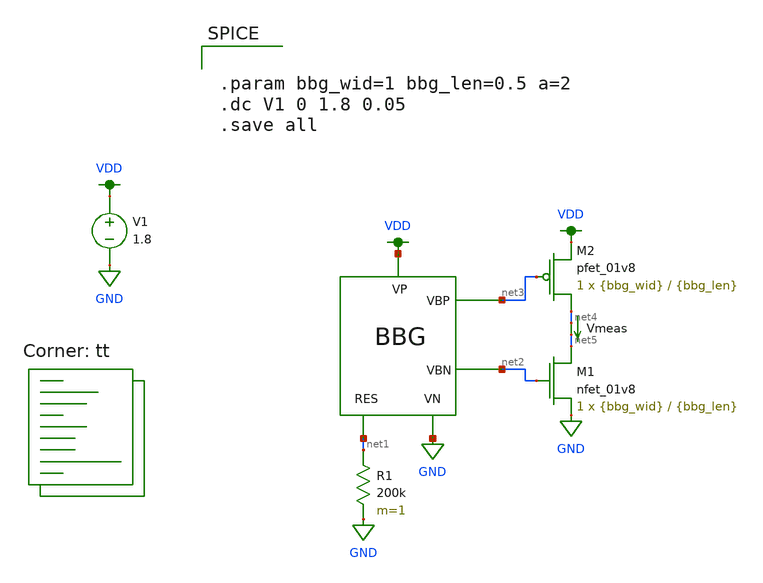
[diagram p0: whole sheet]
** sch_path: test_bbg.sch
**.subckt test_bbg
R1 net1 GND 200k m=1
V1 VDD GND 1.8
XM1 net5 net2 GND GND sky130_fd_pr__nfet_01v8 L={bbg_len} W={bbg_wid} nf=1 ad='int((nf+1)/2) * W/nf * 0.29'
+ as='int((nf+2)/2) * W/nf * 0.29' pd='2*int((nf+1)/2) * (W/nf + 0.29)' ps='2*int((nf+2)/2) * (W/nf + 0.29)'
+ nrd='0.29 / W' nrs='0.29 / W' sa=0 sb=0 sd=0 mult=1 m=1
XM2 net4 net3 VDD VDD sky130_fd_pr__pfet_01v8 L={bbg_len} W={bbg_wid} nf=1 ad='int((nf+1)/2) * W/nf * 0.29'
+ as='int((nf+2)/2) * W/nf * 0.29' pd='2*int((nf+1)/2) * (W/nf + 0.29)' ps='2*int((nf+2)/2) * (W/nf + 0.29)'
+ nrd='0.29 / W' nrs='0.29 / W' sa=0 sb=0 sd=0 mult=1 m=1
Vmeas net4 net5 0
.save i(vmeas)
X1 VDD net1 GND net3 net2 bbg
**** begin user architecture code


.param bbg_wid=1 bbg_len=0.5 a=2
.dc V1 0 1.8 0.05
.save all

.lib $::SKYWATER_MODELS/sky130.lib.spice tt
**** end user architecture code
**.ends

* expanding   symbol:  bbg.sym # of pins=5
** sym_path: bbg.sym
** sch_path: bbg.sch
.subckt bbg VP RES VN VBP VBN
*.iopin VP
*.iopin VN
*.iopin RES
*.opin VBP
*.opin VBN
XM1 net1 net1 RES VN sky130_fd_pr__nfet_01v8 L={bbg_len} W={a}*{bbg_wid} nf=1 ad='int((nf+1)/2) * W/nf * 0.29'
+ as='int((nf+2)/2) * W/nf * 0.29' pd='2*int((nf+1)/2) * (W/nf + 0.29)' ps='2*int((nf+2)/2) * (W/nf + 0.29)'
+ nrd='0.29 / W' nrs='0.29 / W' sa=0 sb=0 sd=0 mult=1 m=1
XM2 net2 net1 VN VN sky130_fd_pr__nfet_01v8 L={bbg_len} W={bbg_wid} nf=1 ad='int((nf+1)/2) * W/nf * 0.29'
+ as='int((nf+2)/2) * W/nf * 0.29' pd='2*int((nf+1)/2) * (W/nf + 0.29)' ps='2*int((nf+2)/2) * (W/nf + 0.29)'
+ nrd='0.29 / W' nrs='0.29 / W' sa=0 sb=0 sd=0 mult=1 m=1
XM3 net1 VBP VP VP sky130_fd_pr__pfet_01v8 L={bbg_len} W={bbg_wid} nf=1 ad='int((nf+1)/2) * W/nf * 0.29'
+ as='int((nf+2)/2) * W/nf * 0.29' pd='2*int((nf+1)/2) * (W/nf + 0.29)' ps='2*int((nf+2)/2) * (W/nf + 0.29)'
+ nrd='0.29 / W' nrs='0.29 / W' sa=0 sb=0 sd=0 mult=1 m=1
Vmeas net3 VBN 0
.save i(vmeas)
XM6 VN VBN VBP VN sky130_fd_pr__nfet_01v8 L={bbg_len} W={bbg_wid} nf=1 ad='int((nf+1)/2) * W/nf * 0.29'
+ as='int((nf+2)/2) * W/nf * 0.29' pd='2*int((nf+1)/2) * (W/nf + 0.29)' ps='2*int((nf+2)/2) * (W/nf + 0.29)'
+ nrd='0.29 / W' nrs='0.29 / W' sa=0 sb=0 sd=0 mult=1 m=1
XM7 VBN VBN VN VN sky130_fd_pr__nfet_01v8 L={bbg_len} W={bbg_wid} nf=1 ad='int((nf+1)/2) * W/nf * 0.29'
+ as='int((nf+2)/2) * W/nf * 0.29' pd='2*int((nf+1)/2) * (W/nf + 0.29)' ps='2*int((nf+2)/2) * (W/nf + 0.29)'
+ nrd='0.29 / W' nrs='0.29 / W' sa=0 sb=0 sd=0 mult=1 m=1
XM4 net2 net2 VP VP sky130_fd_pr__pfet_01v8 L={bbg_len} W={bbg_wid} nf=1 ad='int((nf+1)/2) * W/nf * 0.29'
+ as='int((nf+2)/2) * W/nf * 0.29' pd='2*int((nf+1)/2) * (W/nf + 0.29)' ps='2*int((nf+2)/2) * (W/nf + 0.29)'
+ nrd='0.29 / W' nrs='0.29 / W' sa=0 sb=0 sd=0 mult=1 m=1
XM5 VP net2 VBP VP sky130_fd_pr__pfet_01v8 L={bbg_len} W={bbg_wid} nf=1 ad='int((nf+1)/2) * W/nf * 0.29'
+ as='int((nf+2)/2) * W/nf * 0.29' pd='2*int((nf+1)/2) * (W/nf + 0.29)' ps='2*int((nf+2)/2) * (W/nf + 0.29)'
+ nrd='0.29 / W' nrs='0.29 / W' sa=0 sb=0 sd=0 mult=1 m=1
XM8 VP VBP net3 VP sky130_fd_pr__pfet_01v8 L={bbg_len} W={bbg_wid} nf=1 ad='int((nf+1)/2) * W/nf * 0.29'
+ as='int((nf+2)/2) * W/nf * 0.29' pd='2*int((nf+1)/2) * (W/nf + 0.29)' ps='2*int((nf+2)/2) * (W/nf + 0.29)'
+ nrd='0.29 / W' nrs='0.29 / W' sa=0 sb=0 sd=0 mult=1 m=1
.ends

.GLOBAL GND
.GLOBAL VDD
.end
